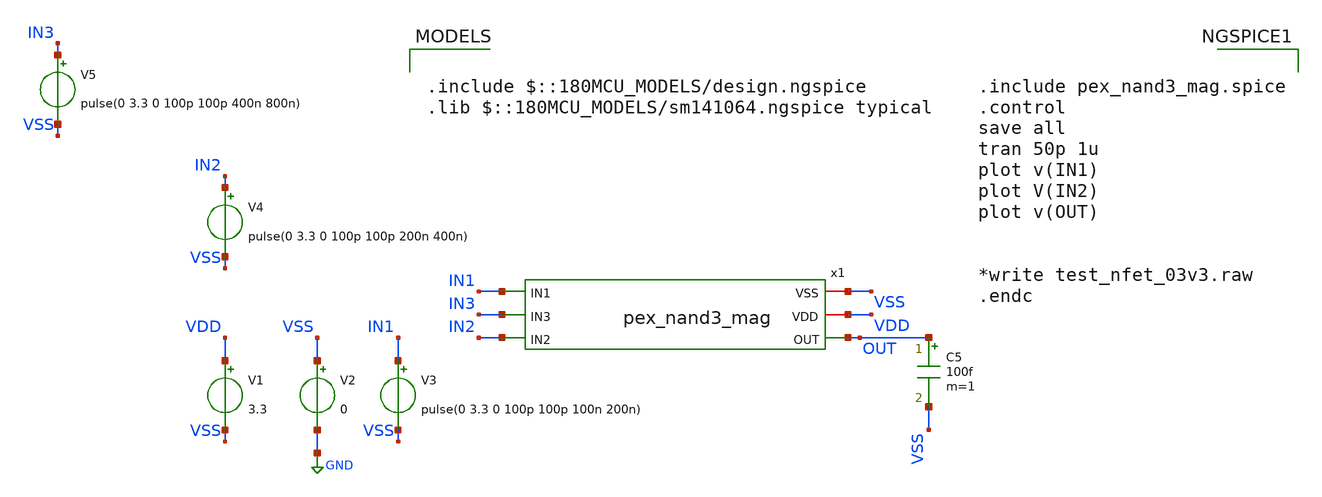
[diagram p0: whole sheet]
** sch_path: Clock_Generator_PAKISTAN_02/Schematics/nand_test_3_pex.sch
**.subckt nand_test_3_pex
V1 VDD VSS 3.3
V2 VSS GND 0
V3 IN1 VSS pulse(0 3.3 0 100p 100p 100n 200n)
V4 IN2 VSS pulse(0 3.3 0 100p 100p 200n 400n)
x1 IN1 VSS VDD OUT IN3 IN2 pex_nand3_mag
V5 IN3 VSS pulse(0 3.3 0 100p 100p 400n 800n)
C5 OUT VSS 100f m=1
**** begin user architecture code

.include $::180MCU_MODELS/design.ngspice
.lib $::180MCU_MODELS/sm141064.ngspice typical



.include pex_nand3_mag.spice
.control
save all
tran 50p 1u
plot v(IN1)
plot V(IN2)
plot v(OUT)


*write test_nfet_03v3.raw
.endc


**** end user architecture code
**.ends
.GLOBAL GND
.end
